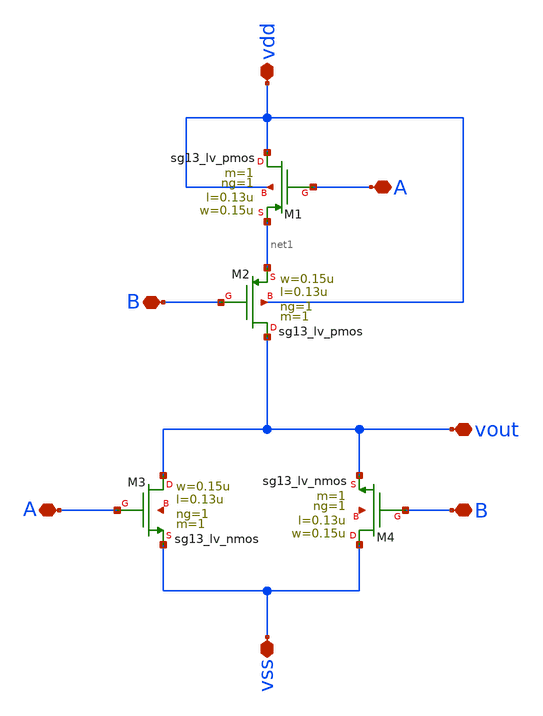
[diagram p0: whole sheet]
** sch_path: design/blocks/puertanor/puertanor.sch
**.subckt puertanor A vdd B vout B vss A
*.iopin A
*.iopin vdd
*.iopin B
*.iopin vout
*.iopin B
*.iopin vss
*.iopin A
XM1 vdd A net1 vdd sg13_lv_pmos w=0.15u l=0.13u ng=1 m=1 mm_ok=1
XM2 vout B net1 vdd sg13_lv_pmos w=0.15u l=0.13u ng=1 m=1 mm_ok=1
XM3 vout A vss net2 sg13_lv_nmos w=0.15u l=0.13u ng=1 m=1 mm_ok=1
XM4 vss B vout net3 sg13_lv_nmos w=0.15u l=0.13u ng=1 m=1 mm_ok=1
**.ends
.end
